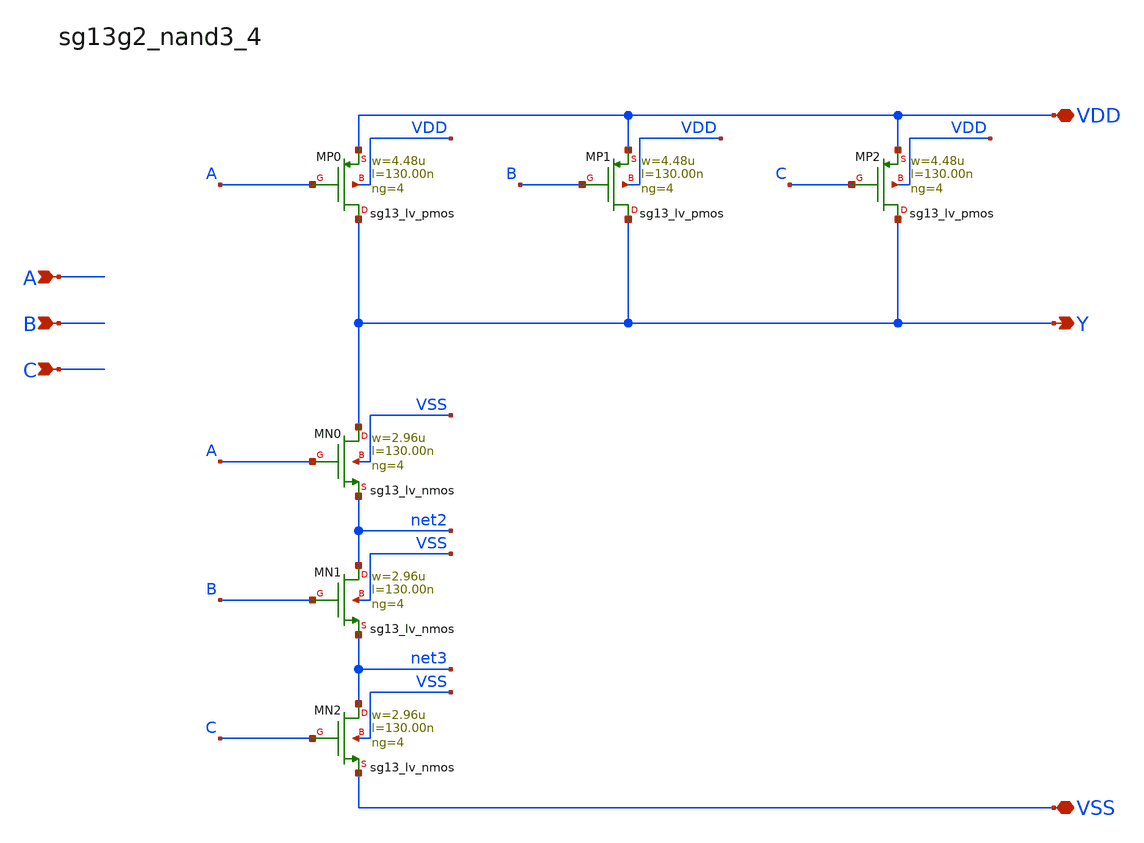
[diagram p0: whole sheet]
** sch_path: outputs/sg13g2_cells/cells/sg13g2_nand3_4/sg13g2_nand3_4.sch
* Copyright 2023  IHP PDK Authors
* Copyright 2024  IHP PDK Authors
**.subckt sg13g2_nand3_4 Y A B C VDD VSS
*.opin Y
*.ipin A
*.ipin B
*.ipin C
*.iopin VDD
*.iopin VSS
XMP0 Y A VDD VDD sg13_lv_pmos w=4.48u l=130.00n ng=4
XMP1 Y B VDD VDD sg13_lv_pmos w=4.48u l=130.00n ng=4
XMP2 Y C VDD VDD sg13_lv_pmos w=4.48u l=130.00n ng=4
XMN1 net2 B net3 VSS sg13_lv_nmos w=2.96u l=130.00n ng=4
XMN2 net3 C VSS VSS sg13_lv_nmos w=2.96u l=130.00n ng=4
XMN0 Y A net2 VSS sg13_lv_nmos w=2.96u l=130.00n ng=4
**.ends
.end
